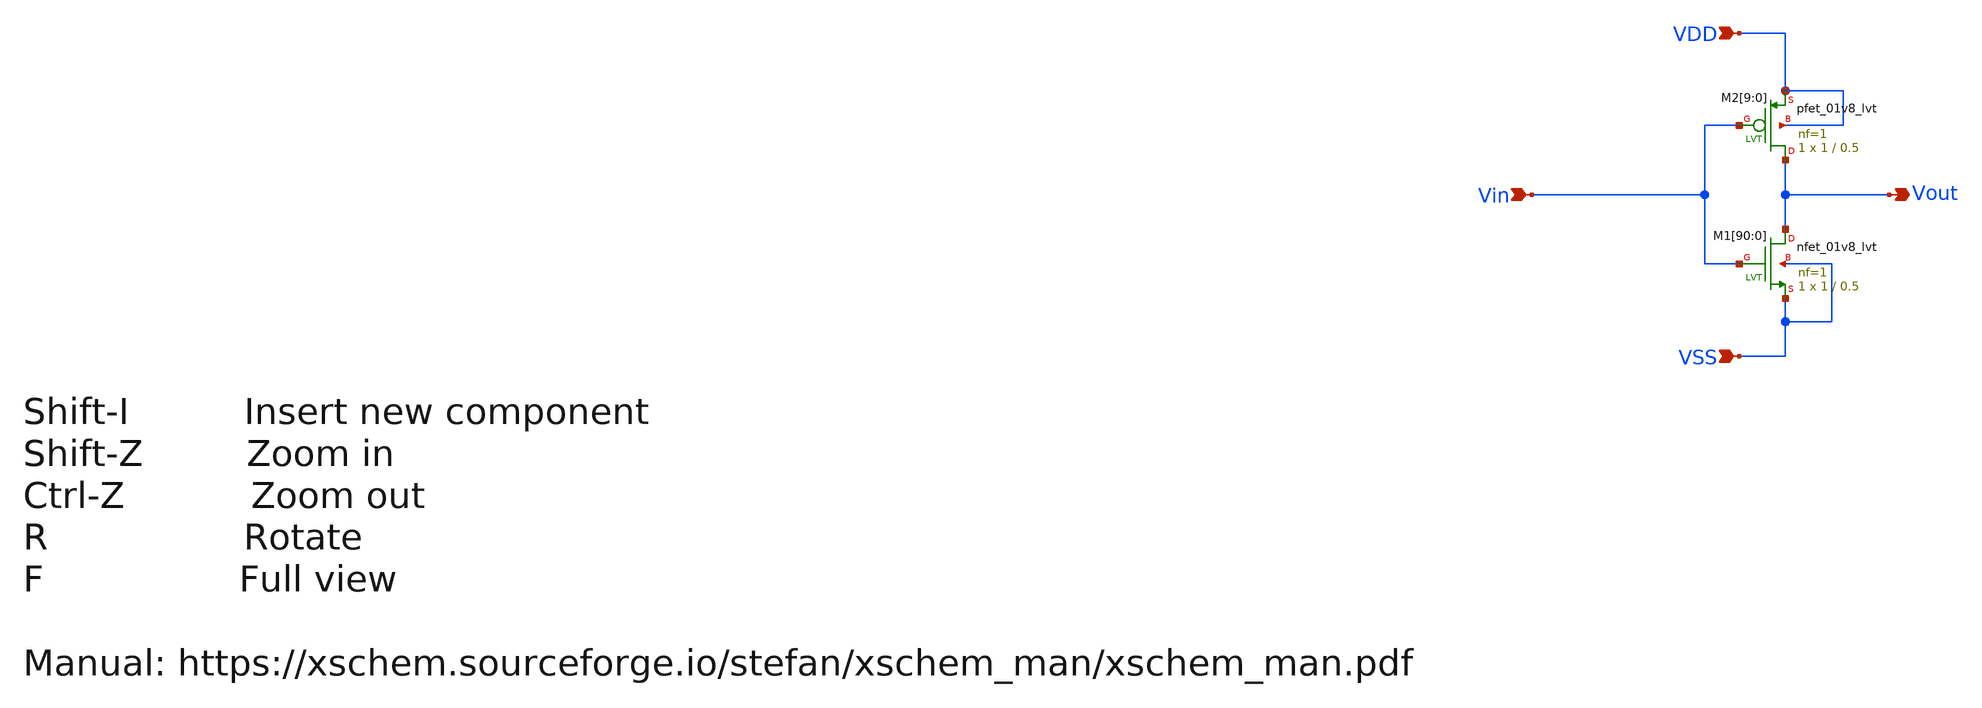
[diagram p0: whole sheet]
** sch_path: design/THESIS_EXP_RO_INVERTER_SKY130A/INV_LVT.sch
**.subckt INV_LVT VDD VSS Vin Vout
*.ipin VDD
*.ipin VSS
*.ipin Vin
*.opin Vout
XM1[90] Vout Vin VSS VSS sky130_fd_pr__nfet_01v8_lvt L=0.5 W=1 nf=1 ad='int((nf+1)/2) * W/nf * 0.29'
+ as='int((nf+2)/2) * W/nf * 0.29' pd='2*int((nf+1)/2) * (W/nf + 0.29)' ps='2*int((nf+2)/2) * (W/nf + 0.29)'
+ nrd='0.29 / W' nrs='0.29 / W' sa=0 sb=0 sd=0 mult=1 m=1
XM1[89] Vout Vin VSS VSS sky130_fd_pr__nfet_01v8_lvt L=0.5 W=1 nf=1 ad='int((nf+1)/2) * W/nf * 0.29'
+ as='int((nf+2)/2) * W/nf * 0.29' pd='2*int((nf+1)/2) * (W/nf + 0.29)' ps='2*int((nf+2)/2) * (W/nf + 0.29)'
+ nrd='0.29 / W' nrs='0.29 / W' sa=0 sb=0 sd=0 mult=1 m=1
XM1[88] Vout Vin VSS VSS sky130_fd_pr__nfet_01v8_lvt L=0.5 W=1 nf=1 ad='int((nf+1)/2) * W/nf * 0.29'
+ as='int((nf+2)/2) * W/nf * 0.29' pd='2*int((nf+1)/2) * (W/nf + 0.29)' ps='2*int((nf+2)/2) * (W/nf + 0.29)'
+ nrd='0.29 / W' nrs='0.29 / W' sa=0 sb=0 sd=0 mult=1 m=1
XM1[87] Vout Vin VSS VSS sky130_fd_pr__nfet_01v8_lvt L=0.5 W=1 nf=1 ad='int((nf+1)/2) * W/nf * 0.29'
+ as='int((nf+2)/2) * W/nf * 0.29' pd='2*int((nf+1)/2) * (W/nf + 0.29)' ps='2*int((nf+2)/2) * (W/nf + 0.29)'
+ nrd='0.29 / W' nrs='0.29 / W' sa=0 sb=0 sd=0 mult=1 m=1
XM1[86] Vout Vin VSS VSS sky130_fd_pr__nfet_01v8_lvt L=0.5 W=1 nf=1 ad='int((nf+1)/2) * W/nf * 0.29'
+ as='int((nf+2)/2) * W/nf * 0.29' pd='2*int((nf+1)/2) * (W/nf + 0.29)' ps='2*int((nf+2)/2) * (W/nf + 0.29)'
+ nrd='0.29 / W' nrs='0.29 / W' sa=0 sb=0 sd=0 mult=1 m=1
XM1[85] Vout Vin VSS VSS sky130_fd_pr__nfet_01v8_lvt L=0.5 W=1 nf=1 ad='int((nf+1)/2) * W/nf * 0.29'
+ as='int((nf+2)/2) * W/nf * 0.29' pd='2*int((nf+1)/2) * (W/nf + 0.29)' ps='2*int((nf+2)/2) * (W/nf + 0.29)'
+ nrd='0.29 / W' nrs='0.29 / W' sa=0 sb=0 sd=0 mult=1 m=1
XM1[84] Vout Vin VSS VSS sky130_fd_pr__nfet_01v8_lvt L=0.5 W=1 nf=1 ad='int((nf+1)/2) * W/nf * 0.29'
+ as='int((nf+2)/2) * W/nf * 0.29' pd='2*int((nf+1)/2) * (W/nf + 0.29)' ps='2*int((nf+2)/2) * (W/nf + 0.29)'
+ nrd='0.29 / W' nrs='0.29 / W' sa=0 sb=0 sd=0 mult=1 m=1
XM1[83] Vout Vin VSS VSS sky130_fd_pr__nfet_01v8_lvt L=0.5 W=1 nf=1 ad='int((nf+1)/2) * W/nf * 0.29'
+ as='int((nf+2)/2) * W/nf * 0.29' pd='2*int((nf+1)/2) * (W/nf + 0.29)' ps='2*int((nf+2)/2) * (W/nf + 0.29)'
+ nrd='0.29 / W' nrs='0.29 / W' sa=0 sb=0 sd=0 mult=1 m=1
XM1[82] Vout Vin VSS VSS sky130_fd_pr__nfet_01v8_lvt L=0.5 W=1 nf=1 ad='int((nf+1)/2) * W/nf * 0.29'
+ as='int((nf+2)/2) * W/nf * 0.29' pd='2*int((nf+1)/2) * (W/nf + 0.29)' ps='2*int((nf+2)/2) * (W/nf + 0.29)'
+ nrd='0.29 / W' nrs='0.29 / W' sa=0 sb=0 sd=0 mult=1 m=1
XM1[81] Vout Vin VSS VSS sky130_fd_pr__nfet_01v8_lvt L=0.5 W=1 nf=1 ad='int((nf+1)/2) * W/nf * 0.29'
+ as='int((nf+2)/2) * W/nf * 0.29' pd='2*int((nf+1)/2) * (W/nf + 0.29)' ps='2*int((nf+2)/2) * (W/nf + 0.29)'
+ nrd='0.29 / W' nrs='0.29 / W' sa=0 sb=0 sd=0 mult=1 m=1
XM1[80] Vout Vin VSS VSS sky130_fd_pr__nfet_01v8_lvt L=0.5 W=1 nf=1 ad='int((nf+1)/2) * W/nf * 0.29'
+ as='int((nf+2)/2) * W/nf * 0.29' pd='2*int((nf+1)/2) * (W/nf + 0.29)' ps='2*int((nf+2)/2) * (W/nf + 0.29)'
+ nrd='0.29 / W' nrs='0.29 / W' sa=0 sb=0 sd=0 mult=1 m=1
XM1[79] Vout Vin VSS VSS sky130_fd_pr__nfet_01v8_lvt L=0.5 W=1 nf=1 ad='int((nf+1)/2) * W/nf * 0.29'
+ as='int((nf+2)/2) * W/nf * 0.29' pd='2*int((nf+1)/2) * (W/nf + 0.29)' ps='2*int((nf+2)/2) * (W/nf + 0.29)'
+ nrd='0.29 / W' nrs='0.29 / W' sa=0 sb=0 sd=0 mult=1 m=1
XM1[78] Vout Vin VSS VSS sky130_fd_pr__nfet_01v8_lvt L=0.5 W=1 nf=1 ad='int((nf+1)/2) * W/nf * 0.29'
+ as='int((nf+2)/2) * W/nf * 0.29' pd='2*int((nf+1)/2) * (W/nf + 0.29)' ps='2*int((nf+2)/2) * (W/nf + 0.29)'
+ nrd='0.29 / W' nrs='0.29 / W' sa=0 sb=0 sd=0 mult=1 m=1
XM1[77] Vout Vin VSS VSS sky130_fd_pr__nfet_01v8_lvt L=0.5 W=1 nf=1 ad='int((nf+1)/2) * W/nf * 0.29'
+ as='int((nf+2)/2) * W/nf * 0.29' pd='2*int((nf+1)/2) * (W/nf + 0.29)' ps='2*int((nf+2)/2) * (W/nf + 0.29)'
+ nrd='0.29 / W' nrs='0.29 / W' sa=0 sb=0 sd=0 mult=1 m=1
XM1[76] Vout Vin VSS VSS sky130_fd_pr__nfet_01v8_lvt L=0.5 W=1 nf=1 ad='int((nf+1)/2) * W/nf * 0.29'
+ as='int((nf+2)/2) * W/nf * 0.29' pd='2*int((nf+1)/2) * (W/nf + 0.29)' ps='2*int((nf+2)/2) * (W/nf + 0.29)'
+ nrd='0.29 / W' nrs='0.29 / W' sa=0 sb=0 sd=0 mult=1 m=1
XM1[75] Vout Vin VSS VSS sky130_fd_pr__nfet_01v8_lvt L=0.5 W=1 nf=1 ad='int((nf+1)/2) * W/nf * 0.29'
+ as='int((nf+2)/2) * W/nf * 0.29' pd='2*int((nf+1)/2) * (W/nf + 0.29)' ps='2*int((nf+2)/2) * (W/nf + 0.29)'
+ nrd='0.29 / W' nrs='0.29 / W' sa=0 sb=0 sd=0 mult=1 m=1
XM1[74] Vout Vin VSS VSS sky130_fd_pr__nfet_01v8_lvt L=0.5 W=1 nf=1 ad='int((nf+1)/2) * W/nf * 0.29'
+ as='int((nf+2)/2) * W/nf * 0.29' pd='2*int((nf+1)/2) * (W/nf + 0.29)' ps='2*int((nf+2)/2) * (W/nf + 0.29)'
+ nrd='0.29 / W' nrs='0.29 / W' sa=0 sb=0 sd=0 mult=1 m=1
XM1[73] Vout Vin VSS VSS sky130_fd_pr__nfet_01v8_lvt L=0.5 W=1 nf=1 ad='int((nf+1)/2) * W/nf * 0.29'
+ as='int((nf+2)/2) * W/nf * 0.29' pd='2*int((nf+1)/2) * (W/nf + 0.29)' ps='2*int((nf+2)/2) * (W/nf + 0.29)'
+ nrd='0.29 / W' nrs='0.29 / W' sa=0 sb=0 sd=0 mult=1 m=1
XM1[72] Vout Vin VSS VSS sky130_fd_pr__nfet_01v8_lvt L=0.5 W=1 nf=1 ad='int((nf+1)/2) * W/nf * 0.29'
+ as='int((nf+2)/2) * W/nf * 0.29' pd='2*int((nf+1)/2) * (W/nf + 0.29)' ps='2*int((nf+2)/2) * (W/nf + 0.29)'
+ nrd='0.29 / W' nrs='0.29 / W' sa=0 sb=0 sd=0 mult=1 m=1
XM1[71] Vout Vin VSS VSS sky130_fd_pr__nfet_01v8_lvt L=0.5 W=1 nf=1 ad='int((nf+1)/2) * W/nf * 0.29'
+ as='int((nf+2)/2) * W/nf * 0.29' pd='2*int((nf+1)/2) * (W/nf + 0.29)' ps='2*int((nf+2)/2) * (W/nf + 0.29)'
+ nrd='0.29 / W' nrs='0.29 / W' sa=0 sb=0 sd=0 mult=1 m=1
XM1[70] Vout Vin VSS VSS sky130_fd_pr__nfet_01v8_lvt L=0.5 W=1 nf=1 ad='int((nf+1)/2) * W/nf * 0.29'
+ as='int((nf+2)/2) * W/nf * 0.29' pd='2*int((nf+1)/2) * (W/nf + 0.29)' ps='2*int((nf+2)/2) * (W/nf + 0.29)'
+ nrd='0.29 / W' nrs='0.29 / W' sa=0 sb=0 sd=0 mult=1 m=1
XM1[69] Vout Vin VSS VSS sky130_fd_pr__nfet_01v8_lvt L=0.5 W=1 nf=1 ad='int((nf+1)/2) * W/nf * 0.29'
+ as='int((nf+2)/2) * W/nf * 0.29' pd='2*int((nf+1)/2) * (W/nf + 0.29)' ps='2*int((nf+2)/2) * (W/nf + 0.29)'
+ nrd='0.29 / W' nrs='0.29 / W' sa=0 sb=0 sd=0 mult=1 m=1
XM1[68] Vout Vin VSS VSS sky130_fd_pr__nfet_01v8_lvt L=0.5 W=1 nf=1 ad='int((nf+1)/2) * W/nf * 0.29'
+ as='int((nf+2)/2) * W/nf * 0.29' pd='2*int((nf+1)/2) * (W/nf + 0.29)' ps='2*int((nf+2)/2) * (W/nf + 0.29)'
+ nrd='0.29 / W' nrs='0.29 / W' sa=0 sb=0 sd=0 mult=1 m=1
XM1[67] Vout Vin VSS VSS sky130_fd_pr__nfet_01v8_lvt L=0.5 W=1 nf=1 ad='int((nf+1)/2) * W/nf * 0.29'
+ as='int((nf+2)/2) * W/nf * 0.29' pd='2*int((nf+1)/2) * (W/nf + 0.29)' ps='2*int((nf+2)/2) * (W/nf + 0.29)'
+ nrd='0.29 / W' nrs='0.29 / W' sa=0 sb=0 sd=0 mult=1 m=1
XM1[66] Vout Vin VSS VSS sky130_fd_pr__nfet_01v8_lvt L=0.5 W=1 nf=1 ad='int((nf+1)/2) * W/nf * 0.29'
+ as='int((nf+2)/2) * W/nf * 0.29' pd='2*int((nf+1)/2) * (W/nf + 0.29)' ps='2*int((nf+2)/2) * (W/nf + 0.29)'
+ nrd='0.29 / W' nrs='0.29 / W' sa=0 sb=0 sd=0 mult=1 m=1
XM1[65] Vout Vin VSS VSS sky130_fd_pr__nfet_01v8_lvt L=0.5 W=1 nf=1 ad='int((nf+1)/2) * W/nf * 0.29'
+ as='int((nf+2)/2) * W/nf * 0.29' pd='2*int((nf+1)/2) * (W/nf + 0.29)' ps='2*int((nf+2)/2) * (W/nf + 0.29)'
+ nrd='0.29 / W' nrs='0.29 / W' sa=0 sb=0 sd=0 mult=1 m=1
XM1[64] Vout Vin VSS VSS sky130_fd_pr__nfet_01v8_lvt L=0.5 W=1 nf=1 ad='int((nf+1)/2) * W/nf * 0.29'
+ as='int((nf+2)/2) * W/nf * 0.29' pd='2*int((nf+1)/2) * (W/nf + 0.29)' ps='2*int((nf+2)/2) * (W/nf + 0.29)'
+ nrd='0.29 / W' nrs='0.29 / W' sa=0 sb=0 sd=0 mult=1 m=1
XM1[63] Vout Vin VSS VSS sky130_fd_pr__nfet_01v8_lvt L=0.5 W=1 nf=1 ad='int((nf+1)/2) * W/nf * 0.29'
+ as='int((nf+2)/2) * W/nf * 0.29' pd='2*int((nf+1)/2) * (W/nf + 0.29)' ps='2*int((nf+2)/2) * (W/nf + 0.29)'
+ nrd='0.29 / W' nrs='0.29 / W' sa=0 sb=0 sd=0 mult=1 m=1
XM1[62] Vout Vin VSS VSS sky130_fd_pr__nfet_01v8_lvt L=0.5 W=1 nf=1 ad='int((nf+1)/2) * W/nf * 0.29'
+ as='int((nf+2)/2) * W/nf * 0.29' pd='2*int((nf+1)/2) * (W/nf + 0.29)' ps='2*int((nf+2)/2) * (W/nf + 0.29)'
+ nrd='0.29 / W' nrs='0.29 / W' sa=0 sb=0 sd=0 mult=1 m=1
XM1[61] Vout Vin VSS VSS sky130_fd_pr__nfet_01v8_lvt L=0.5 W=1 nf=1 ad='int((nf+1)/2) * W/nf * 0.29'
+ as='int((nf+2)/2) * W/nf * 0.29' pd='2*int((nf+1)/2) * (W/nf + 0.29)' ps='2*int((nf+2)/2) * (W/nf + 0.29)'
+ nrd='0.29 / W' nrs='0.29 / W' sa=0 sb=0 sd=0 mult=1 m=1
XM1[60] Vout Vin VSS VSS sky130_fd_pr__nfet_01v8_lvt L=0.5 W=1 nf=1 ad='int((nf+1)/2) * W/nf * 0.29'
+ as='int((nf+2)/2) * W/nf * 0.29' pd='2*int((nf+1)/2) * (W/nf + 0.29)' ps='2*int((nf+2)/2) * (W/nf + 0.29)'
+ nrd='0.29 / W' nrs='0.29 / W' sa=0 sb=0 sd=0 mult=1 m=1
XM1[59] Vout Vin VSS VSS sky130_fd_pr__nfet_01v8_lvt L=0.5 W=1 nf=1 ad='int((nf+1)/2) * W/nf * 0.29'
+ as='int((nf+2)/2) * W/nf * 0.29' pd='2*int((nf+1)/2) * (W/nf + 0.29)' ps='2*int((nf+2)/2) * (W/nf + 0.29)'
+ nrd='0.29 / W' nrs='0.29 / W' sa=0 sb=0 sd=0 mult=1 m=1
XM1[58] Vout Vin VSS VSS sky130_fd_pr__nfet_01v8_lvt L=0.5 W=1 nf=1 ad='int((nf+1)/2) * W/nf * 0.29'
+ as='int((nf+2)/2) * W/nf * 0.29' pd='2*int((nf+1)/2) * (W/nf + 0.29)' ps='2*int((nf+2)/2) * (W/nf + 0.29)'
+ nrd='0.29 / W' nrs='0.29 / W' sa=0 sb=0 sd=0 mult=1 m=1
XM1[57] Vout Vin VSS VSS sky130_fd_pr__nfet_01v8_lvt L=0.5 W=1 nf=1 ad='int((nf+1)/2) * W/nf * 0.29'
+ as='int((nf+2)/2) * W/nf * 0.29' pd='2*int((nf+1)/2) * (W/nf + 0.29)' ps='2*int((nf+2)/2) * (W/nf + 0.29)'
+ nrd='0.29 / W' nrs='0.29 / W' sa=0 sb=0 sd=0 mult=1 m=1
XM1[56] Vout Vin VSS VSS sky130_fd_pr__nfet_01v8_lvt L=0.5 W=1 nf=1 ad='int((nf+1)/2) * W/nf * 0.29'
+ as='int((nf+2)/2) * W/nf * 0.29' pd='2*int((nf+1)/2) * (W/nf + 0.29)' ps='2*int((nf+2)/2) * (W/nf + 0.29)'
+ nrd='0.29 / W' nrs='0.29 / W' sa=0 sb=0 sd=0 mult=1 m=1
XM1[55] Vout Vin VSS VSS sky130_fd_pr__nfet_01v8_lvt L=0.5 W=1 nf=1 ad='int((nf+1)/2) * W/nf * 0.29'
+ as='int((nf+2)/2) * W/nf * 0.29' pd='2*int((nf+1)/2) * (W/nf + 0.29)' ps='2*int((nf+2)/2) * (W/nf + 0.29)'
+ nrd='0.29 / W' nrs='0.29 / W' sa=0 sb=0 sd=0 mult=1 m=1
XM1[54] Vout Vin VSS VSS sky130_fd_pr__nfet_01v8_lvt L=0.5 W=1 nf=1 ad='int((nf+1)/2) * W/nf * 0.29'
+ as='int((nf+2)/2) * W/nf * 0.29' pd='2*int((nf+1)/2) * (W/nf + 0.29)' ps='2*int((nf+2)/2) * (W/nf + 0.29)'
+ nrd='0.29 / W' nrs='0.29 / W' sa=0 sb=0 sd=0 mult=1 m=1
XM1[53] Vout Vin VSS VSS sky130_fd_pr__nfet_01v8_lvt L=0.5 W=1 nf=1 ad='int((nf+1)/2) * W/nf * 0.29'
+ as='int((nf+2)/2) * W/nf * 0.29' pd='2*int((nf+1)/2) * (W/nf + 0.29)' ps='2*int((nf+2)/2) * (W/nf + 0.29)'
+ nrd='0.29 / W' nrs='0.29 / W' sa=0 sb=0 sd=0 mult=1 m=1
XM1[52] Vout Vin VSS VSS sky130_fd_pr__nfet_01v8_lvt L=0.5 W=1 nf=1 ad='int((nf+1)/2) * W/nf * 0.29'
+ as='int((nf+2)/2) * W/nf * 0.29' pd='2*int((nf+1)/2) * (W/nf + 0.29)' ps='2*int((nf+2)/2) * (W/nf + 0.29)'
+ nrd='0.29 / W' nrs='0.29 / W' sa=0 sb=0 sd=0 mult=1 m=1
XM1[51] Vout Vin VSS VSS sky130_fd_pr__nfet_01v8_lvt L=0.5 W=1 nf=1 ad='int((nf+1)/2) * W/nf * 0.29'
+ as='int((nf+2)/2) * W/nf * 0.29' pd='2*int((nf+1)/2) * (W/nf + 0.29)' ps='2*int((nf+2)/2) * (W/nf + 0.29)'
+ nrd='0.29 / W' nrs='0.29 / W' sa=0 sb=0 sd=0 mult=1 m=1
XM1[50] Vout Vin VSS VSS sky130_fd_pr__nfet_01v8_lvt L=0.5 W=1 nf=1 ad='int((nf+1)/2) * W/nf * 0.29'
+ as='int((nf+2)/2) * W/nf * 0.29' pd='2*int((nf+1)/2) * (W/nf + 0.29)' ps='2*int((nf+2)/2) * (W/nf + 0.29)'
+ nrd='0.29 / W' nrs='0.29 / W' sa=0 sb=0 sd=0 mult=1 m=1
XM1[49] Vout Vin VSS VSS sky130_fd_pr__nfet_01v8_lvt L=0.5 W=1 nf=1 ad='int((nf+1)/2) * W/nf * 0.29'
+ as='int((nf+2)/2) * W/nf * 0.29' pd='2*int((nf+1)/2) * (W/nf + 0.29)' ps='2*int((nf+2)/2) * (W/nf + 0.29)'
+ nrd='0.29 / W' nrs='0.29 / W' sa=0 sb=0 sd=0 mult=1 m=1
XM1[48] Vout Vin VSS VSS sky130_fd_pr__nfet_01v8_lvt L=0.5 W=1 nf=1 ad='int((nf+1)/2) * W/nf * 0.29'
+ as='int((nf+2)/2) * W/nf * 0.29' pd='2*int((nf+1)/2) * (W/nf + 0.29)' ps='2*int((nf+2)/2) * (W/nf + 0.29)'
+ nrd='0.29 / W' nrs='0.29 / W' sa=0 sb=0 sd=0 mult=1 m=1
XM1[47] Vout Vin VSS VSS sky130_fd_pr__nfet_01v8_lvt L=0.5 W=1 nf=1 ad='int((nf+1)/2) * W/nf * 0.29'
+ as='int((nf+2)/2) * W/nf * 0.29' pd='2*int((nf+1)/2) * (W/nf + 0.29)' ps='2*int((nf+2)/2) * (W/nf + 0.29)'
+ nrd='0.29 / W' nrs='0.29 / W' sa=0 sb=0 sd=0 mult=1 m=1
XM1[46] Vout Vin VSS VSS sky130_fd_pr__nfet_01v8_lvt L=0.5 W=1 nf=1 ad='int((nf+1)/2) * W/nf * 0.29'
+ as='int((nf+2)/2) * W/nf * 0.29' pd='2*int((nf+1)/2) * (W/nf + 0.29)' ps='2*int((nf+2)/2) * (W/nf + 0.29)'
+ nrd='0.29 / W' nrs='0.29 / W' sa=0 sb=0 sd=0 mult=1 m=1
XM1[45] Vout Vin VSS VSS sky130_fd_pr__nfet_01v8_lvt L=0.5 W=1 nf=1 ad='int((nf+1)/2) * W/nf * 0.29'
+ as='int((nf+2)/2) * W/nf * 0.29' pd='2*int((nf+1)/2) * (W/nf + 0.29)' ps='2*int((nf+2)/2) * (W/nf + 0.29)'
+ nrd='0.29 / W' nrs='0.29 / W' sa=0 sb=0 sd=0 mult=1 m=1
XM1[44] Vout Vin VSS VSS sky130_fd_pr__nfet_01v8_lvt L=0.5 W=1 nf=1 ad='int((nf+1)/2) * W/nf * 0.29'
+ as='int((nf+2)/2) * W/nf * 0.29' pd='2*int((nf+1)/2) * (W/nf + 0.29)' ps='2*int((nf+2)/2) * (W/nf + 0.29)'
+ nrd='0.29 / W' nrs='0.29 / W' sa=0 sb=0 sd=0 mult=1 m=1
XM1[43] Vout Vin VSS VSS sky130_fd_pr__nfet_01v8_lvt L=0.5 W=1 nf=1 ad='int((nf+1)/2) * W/nf * 0.29'
+ as='int((nf+2)/2) * W/nf * 0.29' pd='2*int((nf+1)/2) * (W/nf + 0.29)' ps='2*int((nf+2)/2) * (W/nf + 0.29)'
+ nrd='0.29 / W' nrs='0.29 / W' sa=0 sb=0 sd=0 mult=1 m=1
XM1[42] Vout Vin VSS VSS sky130_fd_pr__nfet_01v8_lvt L=0.5 W=1 nf=1 ad='int((nf+1)/2) * W/nf * 0.29'
+ as='int((nf+2)/2) * W/nf * 0.29' pd='2*int((nf+1)/2) * (W/nf + 0.29)' ps='2*int((nf+2)/2) * (W/nf + 0.29)'
+ nrd='0.29 / W' nrs='0.29 / W' sa=0 sb=0 sd=0 mult=1 m=1
XM1[41] Vout Vin VSS VSS sky130_fd_pr__nfet_01v8_lvt L=0.5 W=1 nf=1 ad='int((nf+1)/2) * W/nf * 0.29'
+ as='int((nf+2)/2) * W/nf * 0.29' pd='2*int((nf+1)/2) * (W/nf + 0.29)' ps='2*int((nf+2)/2) * (W/nf + 0.29)'
+ nrd='0.29 / W' nrs='0.29 / W' sa=0 sb=0 sd=0 mult=1 m=1
XM1[40] Vout Vin VSS VSS sky130_fd_pr__nfet_01v8_lvt L=0.5 W=1 nf=1 ad='int((nf+1)/2) * W/nf * 0.29'
+ as='int((nf+2)/2) * W/nf * 0.29' pd='2*int((nf+1)/2) * (W/nf + 0.29)' ps='2*int((nf+2)/2) * (W/nf + 0.29)'
+ nrd='0.29 / W' nrs='0.29 / W' sa=0 sb=0 sd=0 mult=1 m=1
XM1[39] Vout Vin VSS VSS sky130_fd_pr__nfet_01v8_lvt L=0.5 W=1 nf=1 ad='int((nf+1)/2) * W/nf * 0.29'
+ as='int((nf+2)/2) * W/nf * 0.29' pd='2*int((nf+1)/2) * (W/nf + 0.29)' ps='2*int((nf+2)/2) * (W/nf + 0.29)'
+ nrd='0.29 / W' nrs='0.29 / W' sa=0 sb=0 sd=0 mult=1 m=1
XM1[38] Vout Vin VSS VSS sky130_fd_pr__nfet_01v8_lvt L=0.5 W=1 nf=1 ad='int((nf+1)/2) * W/nf * 0.29'
+ as='int((nf+2)/2) * W/nf * 0.29' pd='2*int((nf+1)/2) * (W/nf + 0.29)' ps='2*int((nf+2)/2) * (W/nf + 0.29)'
+ nrd='0.29 / W' nrs='0.29 / W' sa=0 sb=0 sd=0 mult=1 m=1
XM1[37] Vout Vin VSS VSS sky130_fd_pr__nfet_01v8_lvt L=0.5 W=1 nf=1 ad='int((nf+1)/2) * W/nf * 0.29'
+ as='int((nf+2)/2) * W/nf * 0.29' pd='2*int((nf+1)/2) * (W/nf + 0.29)' ps='2*int((nf+2)/2) * (W/nf + 0.29)'
+ nrd='0.29 / W' nrs='0.29 / W' sa=0 sb=0 sd=0 mult=1 m=1
XM1[36] Vout Vin VSS VSS sky130_fd_pr__nfet_01v8_lvt L=0.5 W=1 nf=1 ad='int((nf+1)/2) * W/nf * 0.29'
+ as='int((nf+2)/2) * W/nf * 0.29' pd='2*int((nf+1)/2) * (W/nf + 0.29)' ps='2*int((nf+2)/2) * (W/nf + 0.29)'
+ nrd='0.29 / W' nrs='0.29 / W' sa=0 sb=0 sd=0 mult=1 m=1
XM1[35] Vout Vin VSS VSS sky130_fd_pr__nfet_01v8_lvt L=0.5 W=1 nf=1 ad='int((nf+1)/2) * W/nf * 0.29'
+ as='int((nf+2)/2) * W/nf * 0.29' pd='2*int((nf+1)/2) * (W/nf + 0.29)' ps='2*int((nf+2)/2) * (W/nf + 0.29)'
+ nrd='0.29 / W' nrs='0.29 / W' sa=0 sb=0 sd=0 mult=1 m=1
XM1[34] Vout Vin VSS VSS sky130_fd_pr__nfet_01v8_lvt L=0.5 W=1 nf=1 ad='int((nf+1)/2) * W/nf * 0.29'
+ as='int((nf+2)/2) * W/nf * 0.29' pd='2*int((nf+1)/2) * (W/nf + 0.29)' ps='2*int((nf+2)/2) * (W/nf + 0.29)'
+ nrd='0.29 / W' nrs='0.29 / W' sa=0 sb=0 sd=0 mult=1 m=1
XM1[33] Vout Vin VSS VSS sky130_fd_pr__nfet_01v8_lvt L=0.5 W=1 nf=1 ad='int((nf+1)/2) * W/nf * 0.29'
+ as='int((nf+2)/2) * W/nf * 0.29' pd='2*int((nf+1)/2) * (W/nf + 0.29)' ps='2*int((nf+2)/2) * (W/nf + 0.29)'
+ nrd='0.29 / W' nrs='0.29 / W' sa=0 sb=0 sd=0 mult=1 m=1
XM1[32] Vout Vin VSS VSS sky130_fd_pr__nfet_01v8_lvt L=0.5 W=1 nf=1 ad='int((nf+1)/2) * W/nf * 0.29'
+ as='int((nf+2)/2) * W/nf * 0.29' pd='2*int((nf+1)/2) * (W/nf + 0.29)' ps='2*int((nf+2)/2) * (W/nf + 0.29)'
+ nrd='0.29 / W' nrs='0.29 / W' sa=0 sb=0 sd=0 mult=1 m=1
XM1[31] Vout Vin VSS VSS sky130_fd_pr__nfet_01v8_lvt L=0.5 W=1 nf=1 ad='int((nf+1)/2) * W/nf * 0.29'
+ as='int((nf+2)/2) * W/nf * 0.29' pd='2*int((nf+1)/2) * (W/nf + 0.29)' ps='2*int((nf+2)/2) * (W/nf + 0.29)'
+ nrd='0.29 / W' nrs='0.29 / W' sa=0 sb=0 sd=0 mult=1 m=1
XM1[30] Vout Vin VSS VSS sky130_fd_pr__nfet_01v8_lvt L=0.5 W=1 nf=1 ad='int((nf+1)/2) * W/nf * 0.29'
+ as='int((nf+2)/2) * W/nf * 0.29' pd='2*int((nf+1)/2) * (W/nf + 0.29)' ps='2*int((nf+2)/2) * (W/nf + 0.29)'
+ nrd='0.29 / W' nrs='0.29 / W' sa=0 sb=0 sd=0 mult=1 m=1
XM1[29] Vout Vin VSS VSS sky130_fd_pr__nfet_01v8_lvt L=0.5 W=1 nf=1 ad='int((nf+1)/2) * W/nf * 0.29'
+ as='int((nf+2)/2) * W/nf * 0.29' pd='2*int((nf+1)/2) * (W/nf + 0.29)' ps='2*int((nf+2)/2) * (W/nf + 0.29)'
+ nrd='0.29 / W' nrs='0.29 / W' sa=0 sb=0 sd=0 mult=1 m=1
XM1[28] Vout Vin VSS VSS sky130_fd_pr__nfet_01v8_lvt L=0.5 W=1 nf=1 ad='int((nf+1)/2) * W/nf * 0.29'
+ as='int((nf+2)/2) * W/nf * 0.29' pd='2*int((nf+1)/2) * (W/nf + 0.29)' ps='2*int((nf+2)/2) * (W/nf + 0.29)'
+ nrd='0.29 / W' nrs='0.29 / W' sa=0 sb=0 sd=0 mult=1 m=1
XM1[27] Vout Vin VSS VSS sky130_fd_pr__nfet_01v8_lvt L=0.5 W=1 nf=1 ad='int((nf+1)/2) * W/nf * 0.29'
+ as='int((nf+2)/2) * W/nf * 0.29' pd='2*int((nf+1)/2) * (W/nf + 0.29)' ps='2*int((nf+2)/2) * (W/nf + 0.29)'
+ nrd='0.29 / W' nrs='0.29 / W' sa=0 sb=0 sd=0 mult=1 m=1
XM1[26] Vout Vin VSS VSS sky130_fd_pr__nfet_01v8_lvt L=0.5 W=1 nf=1 ad='int((nf+1)/2) * W/nf * 0.29'
+ as='int((nf+2)/2) * W/nf * 0.29' pd='2*int((nf+1)/2) * (W/nf + 0.29)' ps='2*int((nf+2)/2) * (W/nf + 0.29)'
+ nrd='0.29 / W' nrs='0.29 / W' sa=0 sb=0 sd=0 mult=1 m=1
XM1[25] Vout Vin VSS VSS sky130_fd_pr__nfet_01v8_lvt L=0.5 W=1 nf=1 ad='int((nf+1)/2) * W/nf * 0.29'
+ as='int((nf+2)/2) * W/nf * 0.29' pd='2*int((nf+1)/2) * (W/nf + 0.29)' ps='2*int((nf+2)/2) * (W/nf + 0.29)'
+ nrd='0.29 / W' nrs='0.29 / W' sa=0 sb=0 sd=0 mult=1 m=1
XM1[24] Vout Vin VSS VSS sky130_fd_pr__nfet_01v8_lvt L=0.5 W=1 nf=1 ad='int((nf+1)/2) * W/nf * 0.29'
+ as='int((nf+2)/2) * W/nf * 0.29' pd='2*int((nf+1)/2) * (W/nf + 0.29)' ps='2*int((nf+2)/2) * (W/nf + 0.29)'
+ nrd='0.29 / W' nrs='0.29 / W' sa=0 sb=0 sd=0 mult=1 m=1
XM1[23] Vout Vin VSS VSS sky130_fd_pr__nfet_01v8_lvt L=0.5 W=1 nf=1 ad='int((nf+1)/2) * W/nf * 0.29'
+ as='int((nf+2)/2) * W/nf * 0.29' pd='2*int((nf+1)/2) * (W/nf + 0.29)' ps='2*int((nf+2)/2) * (W/nf + 0.29)'
+ nrd='0.29 / W' nrs='0.29 / W' sa=0 sb=0 sd=0 mult=1 m=1
XM1[22] Vout Vin VSS VSS sky130_fd_pr__nfet_01v8_lvt L=0.5 W=1 nf=1 ad='int((nf+1)/2) * W/nf * 0.29'
+ as='int((nf+2)/2) * W/nf * 0.29' pd='2*int((nf+1)/2) * (W/nf + 0.29)' ps='2*int((nf+2)/2) * (W/nf + 0.29)'
+ nrd='0.29 / W' nrs='0.29 / W' sa=0 sb=0 sd=0 mult=1 m=1
XM1[21] Vout Vin VSS VSS sky130_fd_pr__nfet_01v8_lvt L=0.5 W=1 nf=1 ad='int((nf+1)/2) * W/nf * 0.29'
+ as='int((nf+2)/2) * W/nf * 0.29' pd='2*int((nf+1)/2) * (W/nf + 0.29)' ps='2*int((nf+2)/2) * (W/nf + 0.29)'
+ nrd='0.29 / W' nrs='0.29 / W' sa=0 sb=0 sd=0 mult=1 m=1
XM1[20] Vout Vin VSS VSS sky130_fd_pr__nfet_01v8_lvt L=0.5 W=1 nf=1 ad='int((nf+1)/2) * W/nf * 0.29'
+ as='int((nf+2)/2) * W/nf * 0.29' pd='2*int((nf+1)/2) * (W/nf + 0.29)' ps='2*int((nf+2)/2) * (W/nf + 0.29)'
+ nrd='0.29 / W' nrs='0.29 / W' sa=0 sb=0 sd=0 mult=1 m=1
XM1[19] Vout Vin VSS VSS sky130_fd_pr__nfet_01v8_lvt L=0.5 W=1 nf=1 ad='int((nf+1)/2) * W/nf * 0.29'
+ as='int((nf+2)/2) * W/nf * 0.29' pd='2*int((nf+1)/2) * (W/nf + 0.29)' ps='2*int((nf+2)/2) * (W/nf + 0.29)'
+ nrd='0.29 / W' nrs='0.29 / W' sa=0 sb=0 sd=0 mult=1 m=1
XM1[18] Vout Vin VSS VSS sky130_fd_pr__nfet_01v8_lvt L=0.5 W=1 nf=1 ad='int((nf+1)/2) * W/nf * 0.29'
+ as='int((nf+2)/2) * W/nf * 0.29' pd='2*int((nf+1)/2) * (W/nf + 0.29)' ps='2*int((nf+2)/2) * (W/nf + 0.29)'
+ nrd='0.29 / W' nrs='0.29 / W' sa=0 sb=0 sd=0 mult=1 m=1
XM1[17] Vout Vin VSS VSS sky130_fd_pr__nfet_01v8_lvt L=0.5 W=1 nf=1 ad='int((nf+1)/2) * W/nf * 0.29'
+ as='int((nf+2)/2) * W/nf * 0.29' pd='2*int((nf+1)/2) * (W/nf + 0.29)' ps='2*int((nf+2)/2) * (W/nf + 0.29)'
+ nrd='0.29 / W' nrs='0.29 / W' sa=0 sb=0 sd=0 mult=1 m=1
XM1[16] Vout Vin VSS VSS sky130_fd_pr__nfet_01v8_lvt L=0.5 W=1 nf=1 ad='int((nf+1)/2) * W/nf * 0.29'
+ as='int((nf+2)/2) * W/nf * 0.29' pd='2*int((nf+1)/2) * (W/nf + 0.29)' ps='2*int((nf+2)/2) * (W/nf + 0.29)'
+ nrd='0.29 / W' nrs='0.29 / W' sa=0 sb=0 sd=0 mult=1 m=1
XM1[15] Vout Vin VSS VSS sky130_fd_pr__nfet_01v8_lvt L=0.5 W=1 nf=1 ad='int((nf+1)/2) * W/nf * 0.29'
+ as='int((nf+2)/2) * W/nf * 0.29' pd='2*int((nf+1)/2) * (W/nf + 0.29)' ps='2*int((nf+2)/2) * (W/nf + 0.29)'
+ nrd='0.29 / W' nrs='0.29 / W' sa=0 sb=0 sd=0 mult=1 m=1
XM1[14] Vout Vin VSS VSS sky130_fd_pr__nfet_01v8_lvt L=0.5 W=1 nf=1 ad='int((nf+1)/2) * W/nf * 0.29'
+ as='int((nf+2)/2) * W/nf * 0.29' pd='2*int((nf+1)/2) * (W/nf + 0.29)' ps='2*int((nf+2)/2) * (W/nf + 0.29)'
+ nrd='0.29 / W' nrs='0.29 / W' sa=0 sb=0 sd=0 mult=1 m=1
XM1[13] Vout Vin VSS VSS sky130_fd_pr__nfet_01v8_lvt L=0.5 W=1 nf=1 ad='int((nf+1)/2) * W/nf * 0.29'
+ as='int((nf+2)/2) * W/nf * 0.29' pd='2*int((nf+1)/2) * (W/nf + 0.29)' ps='2*int((nf+2)/2) * (W/nf + 0.29)'
+ nrd='0.29 / W' nrs='0.29 / W' sa=0 sb=0 sd=0 mult=1 m=1
XM1[12] Vout Vin VSS VSS sky130_fd_pr__nfet_01v8_lvt L=0.5 W=1 nf=1 ad='int((nf+1)/2) * W/nf * 0.29'
+ as='int((nf+2)/2) * W/nf * 0.29' pd='2*int((nf+1)/2) * (W/nf + 0.29)' ps='2*int((nf+2)/2) * (W/nf + 0.29)'
+ nrd='0.29 / W' nrs='0.29 / W' sa=0 sb=0 sd=0 mult=1 m=1
XM1[11] Vout Vin VSS VSS sky130_fd_pr__nfet_01v8_lvt L=0.5 W=1 nf=1 ad='int((nf+1)/2) * W/nf * 0.29'
+ as='int((nf+2)/2) * W/nf * 0.29' pd='2*int((nf+1)/2) * (W/nf + 0.29)' ps='2*int((nf+2)/2) * (W/nf + 0.29)'
+ nrd='0.29 / W' nrs='0.29 / W' sa=0 sb=0 sd=0 mult=1 m=1
XM1[10] Vout Vin VSS VSS sky130_fd_pr__nfet_01v8_lvt L=0.5 W=1 nf=1 ad='int((nf+1)/2) * W/nf * 0.29'
+ as='int((nf+2)/2) * W/nf * 0.29' pd='2*int((nf+1)/2) * (W/nf + 0.29)' ps='2*int((nf+2)/2) * (W/nf + 0.29)'
+ nrd='0.29 / W' nrs='0.29 / W' sa=0 sb=0 sd=0 mult=1 m=1
XM1[9] Vout Vin VSS VSS sky130_fd_pr__nfet_01v8_lvt L=0.5 W=1 nf=1 ad='int((nf+1)/2) * W/nf * 0.29' as='int((nf+2)/2) * W/nf * 0.29'
+ pd='2*int((nf+1)/2) * (W/nf + 0.29)' ps='2*int((nf+2)/2) * (W/nf + 0.29)' nrd='0.29 / W' nrs='0.29 / W'
+ sa=0 sb=0 sd=0 mult=1 m=1
XM1[8] Vout Vin VSS VSS sky130_fd_pr__nfet_01v8_lvt L=0.5 W=1 nf=1 ad='int((nf+1)/2) * W/nf * 0.29' as='int((nf+2)/2) * W/nf * 0.29'
+ pd='2*int((nf+1)/2) * (W/nf + 0.29)' ps='2*int((nf+2)/2) * (W/nf + 0.29)' nrd='0.29 / W' nrs='0.29 / W'
+ sa=0 sb=0 sd=0 mult=1 m=1
XM1[7] Vout Vin VSS VSS sky130_fd_pr__nfet_01v8_lvt L=0.5 W=1 nf=1 ad='int((nf+1)/2) * W/nf * 0.29' as='int((nf+2)/2) * W/nf * 0.29'
+ pd='2*int((nf+1)/2) * (W/nf + 0.29)' ps='2*int((nf+2)/2) * (W/nf + 0.29)' nrd='0.29 / W' nrs='0.29 / W'
+ sa=0 sb=0 sd=0 mult=1 m=1
XM1[6] Vout Vin VSS VSS sky130_fd_pr__nfet_01v8_lvt L=0.5 W=1 nf=1 ad='int((nf+1)/2) * W/nf * 0.29' as='int((nf+2)/2) * W/nf * 0.29'
+ pd='2*int((nf+1)/2) * (W/nf + 0.29)' ps='2*int((nf+2)/2) * (W/nf + 0.29)' nrd='0.29 / W' nrs='0.29 / W'
+ sa=0 sb=0 sd=0 mult=1 m=1
XM1[5] Vout Vin VSS VSS sky130_fd_pr__nfet_01v8_lvt L=0.5 W=1 nf=1 ad='int((nf+1)/2) * W/nf * 0.29' as='int((nf+2)/2) * W/nf * 0.29'
+ pd='2*int((nf+1)/2) * (W/nf + 0.29)' ps='2*int((nf+2)/2) * (W/nf + 0.29)' nrd='0.29 / W' nrs='0.29 / W'
+ sa=0 sb=0 sd=0 mult=1 m=1
XM1[4] Vout Vin VSS VSS sky130_fd_pr__nfet_01v8_lvt L=0.5 W=1 nf=1 ad='int((nf+1)/2) * W/nf * 0.29' as='int((nf+2)/2) * W/nf * 0.29'
+ pd='2*int((nf+1)/2) * (W/nf + 0.29)' ps='2*int((nf+2)/2) * (W/nf + 0.29)' nrd='0.29 / W' nrs='0.29 / W'
+ sa=0 sb=0 sd=0 mult=1 m=1
XM1[3] Vout Vin VSS VSS sky130_fd_pr__nfet_01v8_lvt L=0.5 W=1 nf=1 ad='int((nf+1)/2) * W/nf * 0.29' as='int((nf+2)/2) * W/nf * 0.29'
+ pd='2*int((nf+1)/2) * (W/nf + 0.29)' ps='2*int((nf+2)/2) * (W/nf + 0.29)' nrd='0.29 / W' nrs='0.29 / W'
+ sa=0 sb=0 sd=0 mult=1 m=1
XM1[2] Vout Vin VSS VSS sky130_fd_pr__nfet_01v8_lvt L=0.5 W=1 nf=1 ad='int((nf+1)/2) * W/nf * 0.29' as='int((nf+2)/2) * W/nf * 0.29'
+ pd='2*int((nf+1)/2) * (W/nf + 0.29)' ps='2*int((nf+2)/2) * (W/nf + 0.29)' nrd='0.29 / W' nrs='0.29 / W'
+ sa=0 sb=0 sd=0 mult=1 m=1
XM1[1] Vout Vin VSS VSS sky130_fd_pr__nfet_01v8_lvt L=0.5 W=1 nf=1 ad='int((nf+1)/2) * W/nf * 0.29' as='int((nf+2)/2) * W/nf * 0.29'
+ pd='2*int((nf+1)/2) * (W/nf + 0.29)' ps='2*int((nf+2)/2) * (W/nf + 0.29)' nrd='0.29 / W' nrs='0.29 / W'
+ sa=0 sb=0 sd=0 mult=1 m=1
XM1[0] Vout Vin VSS VSS sky130_fd_pr__nfet_01v8_lvt L=0.5 W=1 nf=1 ad='int((nf+1)/2) * W/nf * 0.29' as='int((nf+2)/2) * W/nf * 0.29'
+ pd='2*int((nf+1)/2) * (W/nf + 0.29)' ps='2*int((nf+2)/2) * (W/nf + 0.29)' nrd='0.29 / W' nrs='0.29 / W'
+ sa=0 sb=0 sd=0 mult=1 m=1
XM2[9] Vout Vin VDD VDD sky130_fd_pr__pfet_01v8_lvt L=0.5 W=1 nf=1 ad='int((nf+1)/2) * W/nf * 0.29' as='int((nf+2)/2) * W/nf * 0.29'
+ pd='2*int((nf+1)/2) * (W/nf + 0.29)' ps='2*int((nf+2)/2) * (W/nf + 0.29)' nrd='0.29 / W' nrs='0.29 / W'
+ sa=0 sb=0 sd=0 mult=1 m=1
XM2[8] Vout Vin VDD VDD sky130_fd_pr__pfet_01v8_lvt L=0.5 W=1 nf=1 ad='int((nf+1)/2) * W/nf * 0.29' as='int((nf+2)/2) * W/nf * 0.29'
+ pd='2*int((nf+1)/2) * (W/nf + 0.29)' ps='2*int((nf+2)/2) * (W/nf + 0.29)' nrd='0.29 / W' nrs='0.29 / W'
+ sa=0 sb=0 sd=0 mult=1 m=1
XM2[7] Vout Vin VDD VDD sky130_fd_pr__pfet_01v8_lvt L=0.5 W=1 nf=1 ad='int((nf+1)/2) * W/nf * 0.29' as='int((nf+2)/2) * W/nf * 0.29'
+ pd='2*int((nf+1)/2) * (W/nf + 0.29)' ps='2*int((nf+2)/2) * (W/nf + 0.29)' nrd='0.29 / W' nrs='0.29 / W'
+ sa=0 sb=0 sd=0 mult=1 m=1
XM2[6] Vout Vin VDD VDD sky130_fd_pr__pfet_01v8_lvt L=0.5 W=1 nf=1 ad='int((nf+1)/2) * W/nf * 0.29' as='int((nf+2)/2) * W/nf * 0.29'
+ pd='2*int((nf+1)/2) * (W/nf + 0.29)' ps='2*int((nf+2)/2) * (W/nf + 0.29)' nrd='0.29 / W' nrs='0.29 / W'
+ sa=0 sb=0 sd=0 mult=1 m=1
XM2[5] Vout Vin VDD VDD sky130_fd_pr__pfet_01v8_lvt L=0.5 W=1 nf=1 ad='int((nf+1)/2) * W/nf * 0.29' as='int((nf+2)/2) * W/nf * 0.29'
+ pd='2*int((nf+1)/2) * (W/nf + 0.29)' ps='2*int((nf+2)/2) * (W/nf + 0.29)' nrd='0.29 / W' nrs='0.29 / W'
+ sa=0 sb=0 sd=0 mult=1 m=1
XM2[4] Vout Vin VDD VDD sky130_fd_pr__pfet_01v8_lvt L=0.5 W=1 nf=1 ad='int((nf+1)/2) * W/nf * 0.29' as='int((nf+2)/2) * W/nf * 0.29'
+ pd='2*int((nf+1)/2) * (W/nf + 0.29)' ps='2*int((nf+2)/2) * (W/nf + 0.29)' nrd='0.29 / W' nrs='0.29 / W'
+ sa=0 sb=0 sd=0 mult=1 m=1
XM2[3] Vout Vin VDD VDD sky130_fd_pr__pfet_01v8_lvt L=0.5 W=1 nf=1 ad='int((nf+1)/2) * W/nf * 0.29' as='int((nf+2)/2) * W/nf * 0.29'
+ pd='2*int((nf+1)/2) * (W/nf + 0.29)' ps='2*int((nf+2)/2) * (W/nf + 0.29)' nrd='0.29 / W' nrs='0.29 / W'
+ sa=0 sb=0 sd=0 mult=1 m=1
XM2[2] Vout Vin VDD VDD sky130_fd_pr__pfet_01v8_lvt L=0.5 W=1 nf=1 ad='int((nf+1)/2) * W/nf * 0.29' as='int((nf+2)/2) * W/nf * 0.29'
+ pd='2*int((nf+1)/2) * (W/nf + 0.29)' ps='2*int((nf+2)/2) * (W/nf + 0.29)' nrd='0.29 / W' nrs='0.29 / W'
+ sa=0 sb=0 sd=0 mult=1 m=1
XM2[1] Vout Vin VDD VDD sky130_fd_pr__pfet_01v8_lvt L=0.5 W=1 nf=1 ad='int((nf+1)/2) * W/nf * 0.29' as='int((nf+2)/2) * W/nf * 0.29'
+ pd='2*int((nf+1)/2) * (W/nf + 0.29)' ps='2*int((nf+2)/2) * (W/nf + 0.29)' nrd='0.29 / W' nrs='0.29 / W'
+ sa=0 sb=0 sd=0 mult=1 m=1
XM2[0] Vout Vin VDD VDD sky130_fd_pr__pfet_01v8_lvt L=0.5 W=1 nf=1 ad='int((nf+1)/2) * W/nf * 0.29' as='int((nf+2)/2) * W/nf * 0.29'
+ pd='2*int((nf+1)/2) * (W/nf + 0.29)' ps='2*int((nf+2)/2) * (W/nf + 0.29)' nrd='0.29 / W' nrs='0.29 / W'
+ sa=0 sb=0 sd=0 mult=1 m=1
**.ends
.end
